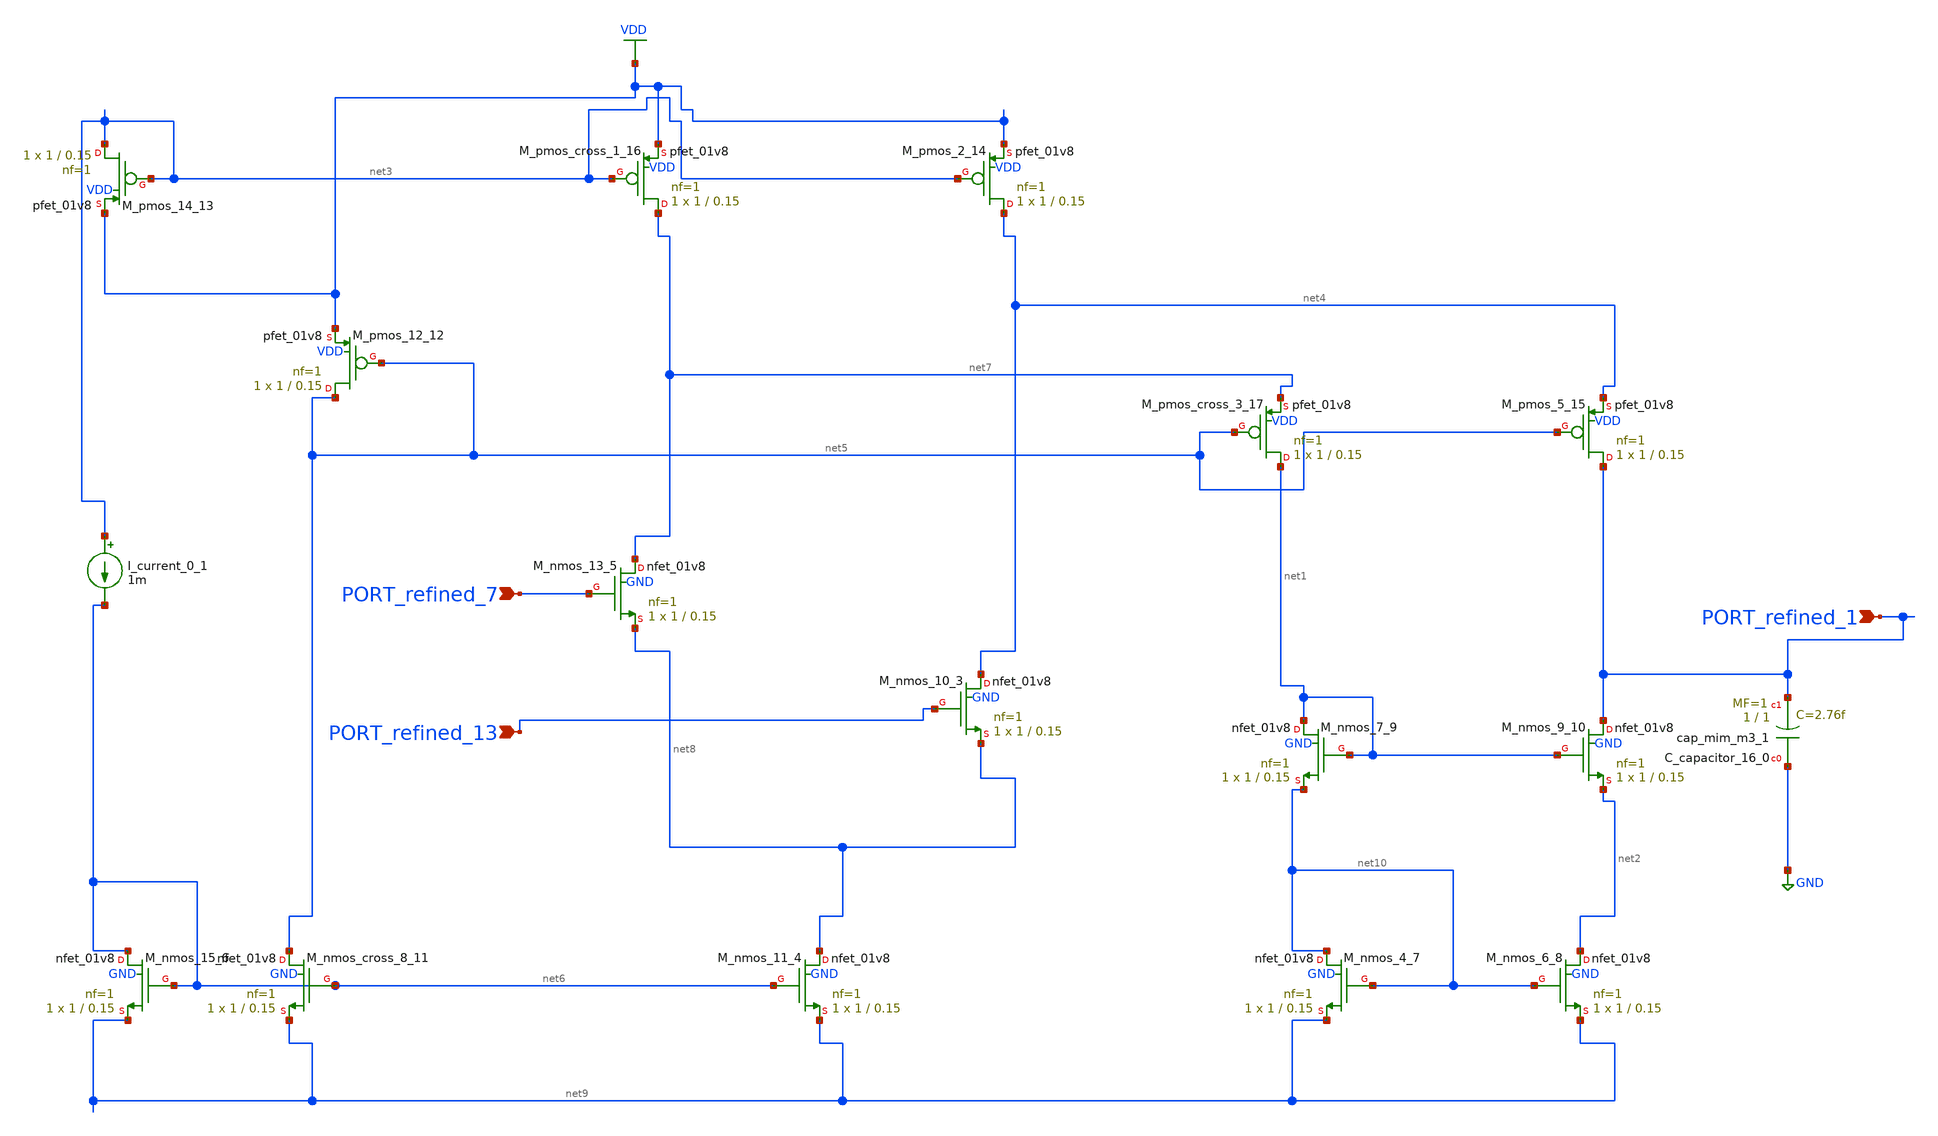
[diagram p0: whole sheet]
** sch_path: schematics/Image2Net/048.sch
**.subckt 048 PORT_refined_13 PORT_refined_7 PORT_refined_1
*.ipin PORT_refined_13
*.ipin PORT_refined_7
*.ipin PORT_refined_1
XC_capacitor_16_0 GND PORT_refined_1 sky130_fd_pr__cap_mim_m3_1 W=1 L=1 MF=1 m=1
I_current_0_1 net3 net6 1m
XM_nmos_10_3 net4 PORT_refined_13 net8 GND sky130_fd_pr__nfet_01v8 L=0.15 W=1 nf=1 ad='int((1 + 1)/2) * 1 / 1 * 0.29'
+ as='int((1 + 2)/2) * 1 / 1 * 0.29' pd='2*int((1 + 1)/2) * (1 / 1 + 0.29)' ps='2*int((1 + 2)/2) * (1 / 1 + 0.29)'
+ nrd='0.29 / 1 ' nrs='0.29 / 1 ' sa=0 sb=0 sd=0 mult=1 m=1
XM_nmos_11_4 net8 net6 net9 GND sky130_fd_pr__nfet_01v8 L=0.15 W=1 nf=1 ad='int((1 + 1)/2) * 1 / 1 * 0.29'
+ as='int((1 + 2)/2) * 1 / 1 * 0.29' pd='2*int((1 + 1)/2) * (1 / 1 + 0.29)' ps='2*int((1 + 2)/2) * (1 / 1 + 0.29)'
+ nrd='0.29 / 1 ' nrs='0.29 / 1 ' sa=0 sb=0 sd=0 mult=1 m=1
XM_nmos_13_5 net7 PORT_refined_7 net8 GND sky130_fd_pr__nfet_01v8 L=0.15 W=1 nf=1 ad='int((1 + 1)/2) * 1 / 1 * 0.29'
+ as='int((1 + 2)/2) * 1 / 1 * 0.29' pd='2*int((1 + 1)/2) * (1 / 1 + 0.29)' ps='2*int((1 + 2)/2) * (1 / 1 + 0.29)'
+ nrd='0.29 / 1 ' nrs='0.29 / 1 ' sa=0 sb=0 sd=0 mult=1 m=1
XM_nmos_15_6 net6 net6 net9 GND sky130_fd_pr__nfet_01v8 L=0.15 W=1 nf=1 ad='int((1 + 1)/2) * 1 / 1 * 0.29'
+ as='int((1 + 2)/2) * 1 / 1 * 0.29' pd='2*int((1 + 1)/2) * (1 / 1 + 0.29)' ps='2*int((1 + 2)/2) * (1 / 1 + 0.29)'
+ nrd='0.29 / 1 ' nrs='0.29 / 1 ' sa=0 sb=0 sd=0 mult=1 m=1
XM_nmos_4_7 net10 net10 net9 GND sky130_fd_pr__nfet_01v8 L=0.15 W=1 nf=1 ad='int((1 + 1)/2) * 1 / 1 * 0.29'
+ as='int((1 + 2)/2) * 1 / 1 * 0.29' pd='2*int((1 + 1)/2) * (1 / 1 + 0.29)' ps='2*int((1 + 2)/2) * (1 / 1 + 0.29)'
+ nrd='0.29 / 1 ' nrs='0.29 / 1 ' sa=0 sb=0 sd=0 mult=1 m=1
XM_nmos_6_8 net2 net10 net9 GND sky130_fd_pr__nfet_01v8 L=0.15 W=1 nf=1 ad='int((1 + 1)/2) * 1 / 1 * 0.29'
+ as='int((1 + 2)/2) * 1 / 1 * 0.29' pd='2*int((1 + 1)/2) * (1 / 1 + 0.29)' ps='2*int((1 + 2)/2) * (1 / 1 + 0.29)'
+ nrd='0.29 / 1 ' nrs='0.29 / 1 ' sa=0 sb=0 sd=0 mult=1 m=1
XM_nmos_7_9 net1 net1 net10 GND sky130_fd_pr__nfet_01v8 L=0.15 W=1 nf=1 ad='int((1 + 1)/2) * 1 / 1 * 0.29'
+ as='int((1 + 2)/2) * 1 / 1 * 0.29' pd='2*int((1 + 1)/2) * (1 / 1 + 0.29)' ps='2*int((1 + 2)/2) * (1 / 1 + 0.29)'
+ nrd='0.29 / 1 ' nrs='0.29 / 1 ' sa=0 sb=0 sd=0 mult=1 m=1
XM_nmos_9_10 PORT_refined_1 net1 net2 GND sky130_fd_pr__nfet_01v8 L=0.15 W=1 nf=1 ad='int((1 + 1)/2) * 1 / 1 * 0.29'
+ as='int((1 + 2)/2) * 1 / 1 * 0.29' pd='2*int((1 + 1)/2) * (1 / 1 + 0.29)' ps='2*int((1 + 2)/2) * (1 / 1 + 0.29)'
+ nrd='0.29 / 1 ' nrs='0.29 / 1 ' sa=0 sb=0 sd=0 mult=1 m=1
XM_nmos_cross_8_11 net5 net6 net9 GND sky130_fd_pr__nfet_01v8 L=0.15 W=1 nf=1 ad='int((1 + 1)/2) * 1 / 1 * 0.29'
+ as='int((1 + 2)/2) * 1 / 1 * 0.29' pd='2*int((1 + 1)/2) * (1 / 1 + 0.29)' ps='2*int((1 + 2)/2) * (1 / 1 + 0.29)'
+ nrd='0.29 / 1 ' nrs='0.29 / 1 ' sa=0 sb=0 sd=0 mult=1 m=1
XM_pmos_12_12 net5 net5 VDD VDD sky130_fd_pr__pfet_01v8 L=0.15 W=1 nf=1 ad='int((1 + 1)/2) * 1 / 1 * 0.29'
+ as='int((1 + 2)/2) * 1 / 1 * 0.29' pd='2*int((1 + 1)/2) * (1 / 1 + 0.29)' ps='2*int((1 + 2)/2) * (1 / 1 + 0.29)'
+ nrd='0.29 / 1 ' nrs='0.29 / 1 ' sa=0 sb=0 sd=0 mult=1 m=1
XM_pmos_14_13 net3 net3 VDD VDD sky130_fd_pr__pfet_01v8 L=0.15 W=1 nf=1 ad='int((1 + 1)/2) * 1 / 1 * 0.29'
+ as='int((1 + 2)/2) * 1 / 1 * 0.29' pd='2*int((1 + 1)/2) * (1 / 1 + 0.29)' ps='2*int((1 + 2)/2) * (1 / 1 + 0.29)'
+ nrd='0.29 / 1 ' nrs='0.29 / 1 ' sa=0 sb=0 sd=0 mult=1 m=1
XM_pmos_2_14 net4 net3 VDD VDD sky130_fd_pr__pfet_01v8 L=0.15 W=1 nf=1 ad='int((1 + 1)/2) * 1 / 1 * 0.29'
+ as='int((1 + 2)/2) * 1 / 1 * 0.29' pd='2*int((1 + 1)/2) * (1 / 1 + 0.29)' ps='2*int((1 + 2)/2) * (1 / 1 + 0.29)'
+ nrd='0.29 / 1 ' nrs='0.29 / 1 ' sa=0 sb=0 sd=0 mult=1 m=1
XM_pmos_5_15 PORT_refined_1 net5 net4 VDD sky130_fd_pr__pfet_01v8 L=0.15 W=1 nf=1 ad='int((1 + 1)/2) * 1 / 1 * 0.29'
+ as='int((1 + 2)/2) * 1 / 1 * 0.29' pd='2*int((1 + 1)/2) * (1 / 1 + 0.29)' ps='2*int((1 + 2)/2) * (1 / 1 + 0.29)'
+ nrd='0.29 / 1 ' nrs='0.29 / 1 ' sa=0 sb=0 sd=0 mult=1 m=1
XM_pmos_cross_1_16 net7 net3 VDD VDD sky130_fd_pr__pfet_01v8 L=0.15 W=1 nf=1 ad='int((1 + 1)/2) * 1 / 1 * 0.29'
+ as='int((1 + 2)/2) * 1 / 1 * 0.29' pd='2*int((1 + 1)/2) * (1 / 1 + 0.29)' ps='2*int((1 + 2)/2) * (1 / 1 + 0.29)'
+ nrd='0.29 / 1 ' nrs='0.29 / 1 ' sa=0 sb=0 sd=0 mult=1 m=1
XM_pmos_cross_3_17 net1 net5 net7 VDD sky130_fd_pr__pfet_01v8 L=0.15 W=1 nf=1 ad='int((1 + 1)/2) * 1 / 1 * 0.29'
+ as='int((1 + 2)/2) * 1 / 1 * 0.29' pd='2*int((1 + 1)/2) * (1 / 1 + 0.29)' ps='2*int((1 + 2)/2) * (1 / 1 + 0.29)'
+ nrd='0.29 / 1 ' nrs='0.29 / 1 ' sa=0 sb=0 sd=0 mult=1 m=1
**.ends
.GLOBAL GND
.GLOBAL VDD
.end
